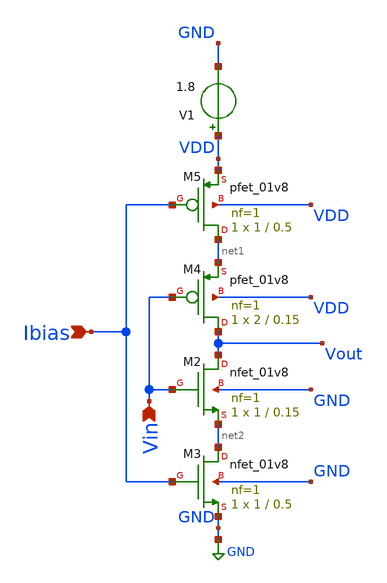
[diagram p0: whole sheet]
** sch_path: csi_cell/csi_cell.sch
**.subckt csi_cell Vin Ibias
*.ipin Vin
*.ipin Ibias
XM2 Vout Vin net2 GND sky130_fd_pr__nfet_01v8 L=0.15 W=1 nf=1 ad='int((1 + 1)/2) * 1 / 1 * 0.29' as='int((1 + 2)/2) * 1 / 1 * 0.29'
+ pd='2*int((1 + 1)/2) * (1 / 1 + 0.29)' ps='2*int((1 + 2)/2) * (1 / 1 + 0.29)' nrd='0.29 / 1 ' nrs='0.29 / 1 '
+ sa=0 sb=0 sd=0 mult=1 m=1
XM3 net2 Ibias GND GND sky130_fd_pr__nfet_01v8 L=0.5 W=1 nf=1 ad='int((1 + 1)/2) * 1 / 1 * 0.29' as='int((1 + 2)/2) * 1 / 1 * 0.29'
+ pd='2*int((1 + 1)/2) * (1 / 1 + 0.29)' ps='2*int((1 + 2)/2) * (1 / 1 + 0.29)' nrd='0.29 / 1 ' nrs='0.29 / 1 '
+ sa=0 sb=0 sd=0 mult=1 m=1
XM4 Vout Vin net1 VDD sky130_fd_pr__pfet_01v8 L=0.15 W=2 nf=1 ad='int((1 + 1)/2) * 2 / 1 * 0.29' as='int((1 + 2)/2) * 2 / 1 * 0.29'
+ pd='2*int((1 + 1)/2) * (2 / 1 + 0.29)' ps='2*int((1 + 2)/2) * (2 / 1 + 0.29)' nrd='0.29 / 2 ' nrs='0.29 / 2 '
+ sa=0 sb=0 sd=0 mult=1 m=1
XM5 net1 Ibias VDD VDD sky130_fd_pr__pfet_01v8 L=0.5 W=1 nf=1 ad='int((1 + 1)/2) * 1 / 1 * 0.29' as='int((1 + 2)/2) * 1 / 1 * 0.29'
+ pd='2*int((1 + 1)/2) * (1 / 1 + 0.29)' ps='2*int((1 + 2)/2) * (1 / 1 + 0.29)' nrd='0.29 / 1 ' nrs='0.29 / 1 '
+ sa=0 sb=0 sd=0 mult=1 m=1
V1 VDD GND 1.8
**.ends
.GLOBAL GND
.end
